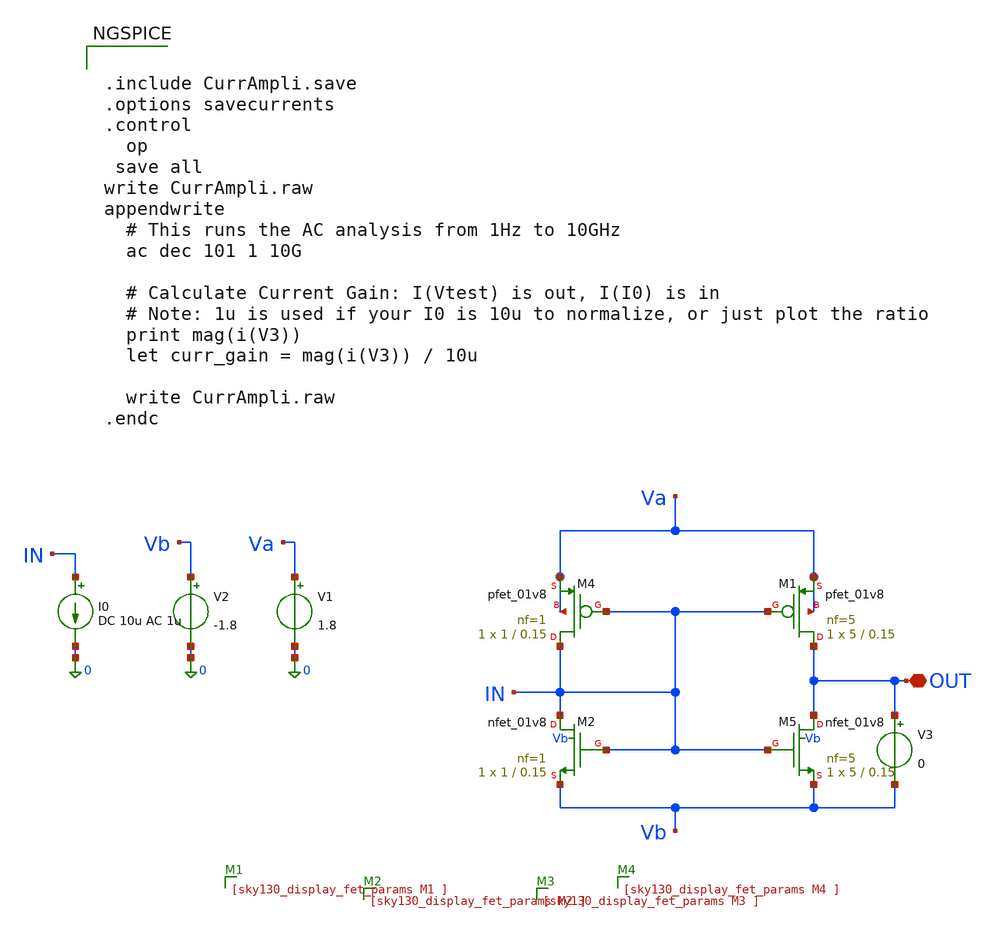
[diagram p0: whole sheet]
** sch_path: design_data/test_xschem_sky130/CurrAmpli.sch
**.subckt CurrAmpli OUT
*.iopin OUT
V1 Va 0 1.8
V2 Vb 0 -1.8
I0 IN 0 DC 10u AC 1u
XM5 OUT IN Vb Vb sky130_fd_pr__nfet_01v8 L=0.15 W=5 nf=5 ad='int((5 + 1)/2) * 5 / 5 * 0.29' as='int((5 + 2)/2) * 5 / 5 * 0.29'
+ pd='2*int((5 + 1)/2) * (5 / 5 + 0.29)' ps='2*int((5 + 2)/2) * (5 / 5 + 0.29)' nrd='0.29 / 5 ' nrs='0.29 / 5 '
+ sa=0 sb=0 sd=0 mult=1 m=1
XM2 IN IN Vb Vb sky130_fd_pr__nfet_01v8 L=0.15 W=1 nf=1 ad='int((1 + 1)/2) * 1 / 1 * 0.29' as='int((1 + 2)/2) * 1 / 1 * 0.29'
+ pd='2*int((1 + 1)/2) * (1 / 1 + 0.29)' ps='2*int((1 + 2)/2) * (1 / 1 + 0.29)' nrd='0.29 / 1 ' nrs='0.29 / 1 '
+ sa=0 sb=0 sd=0 mult=1 m=1
XM1 OUT IN Va Va sky130_fd_pr__pfet_01v8 L=0.15 W=5 nf=5 ad='int((5 + 1)/2) * 5 / 5 * 0.29' as='int((5 + 2)/2) * 5 / 5 * 0.29'
+ pd='2*int((5 + 1)/2) * (5 / 5 + 0.29)' ps='2*int((5 + 2)/2) * (5 / 5 + 0.29)' nrd='0.29 / 5 ' nrs='0.29 / 5 '
+ sa=0 sb=0 sd=0 mult=1 m=1
XM4 IN IN Va Va sky130_fd_pr__pfet_01v8 L=0.15 W=1 nf=1 ad='int((1 + 1)/2) * 1 / 1 * 0.29' as='int((1 + 2)/2) * 1 / 1 * 0.29'
+ pd='2*int((1 + 1)/2) * (1 / 1 + 0.29)' ps='2*int((1 + 2)/2) * (1 / 1 + 0.29)' nrd='0.29 / 1 ' nrs='0.29 / 1 '
+ sa=0 sb=0 sd=0 mult=1 m=1
V3 OUT Vb 0
**** begin user architecture code

** opencircuitdesign pdks install
.lib $::SKYWATER_MODELS/sky130.lib.spice tt



.include CurrAmpli.save
.options savecurrents
.control
  op
 save all
write CurrAmpli.raw
appendwrite
  # This runs the AC analysis from 1Hz to 10GHz
  ac dec 101 1 10G

  # Calculate Current Gain: I(Vtest) is out, I(I0) is in
  # Note: 1u is used if your I0 is 10u to normalize, or just plot the ratio
  print mag(i(V3))
  let curr_gain = mag(i(V3)) / 10u

  write CurrAmpli.raw
.endc


**** end user architecture code
**.ends
.end
